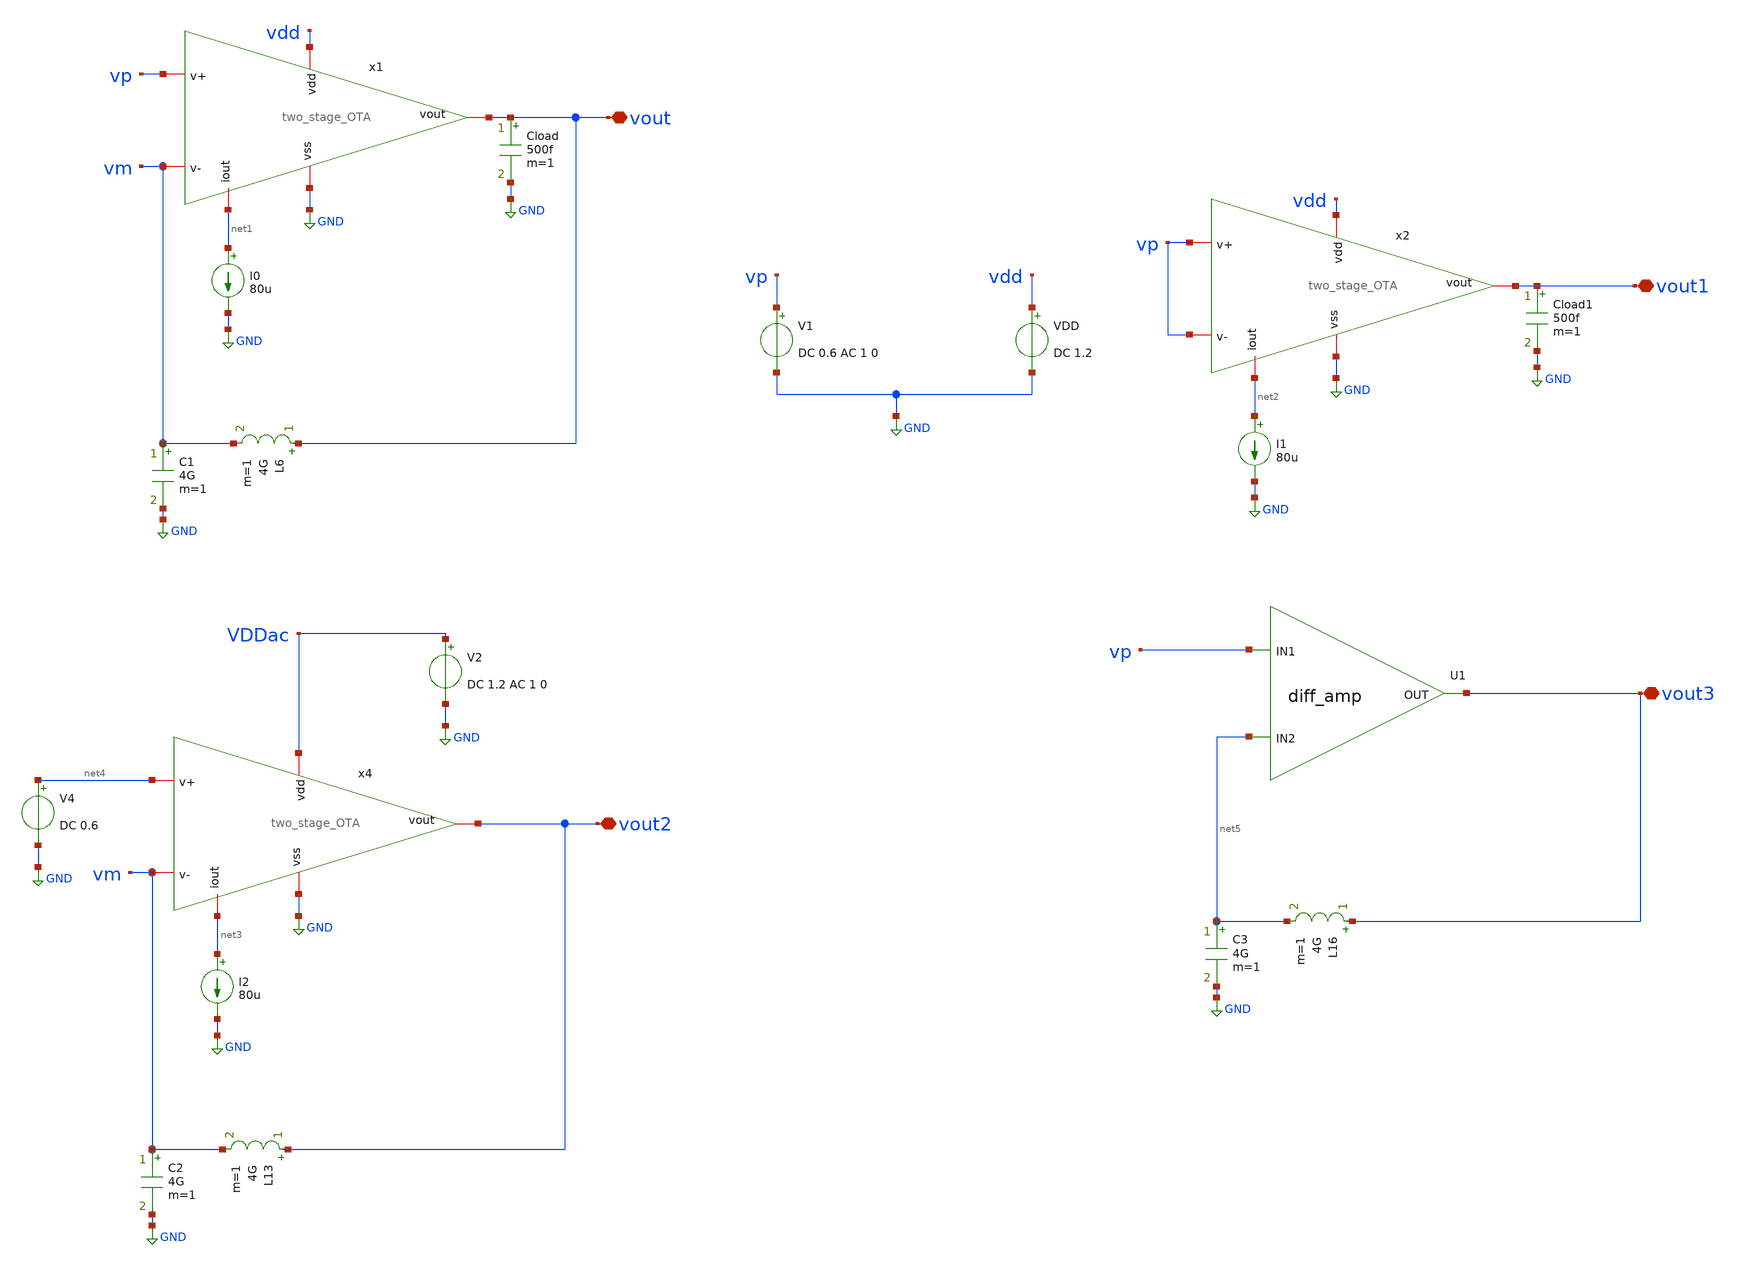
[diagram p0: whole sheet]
** sch_path: modules/module_1_bandgap_reference/part_1_OTA/testbenches/ota_testbench.sch
**.subckt ota_testbench vout vout1 vout2 vout3
*.iopin vout
*.iopin vout1
*.iopin vout2
*.iopin vout3
V1 vp GND DC 0.6 AC 1 0
VDD vdd GND DC 1.2
I0 net1 GND 80u
Cload vout GND 500f m=1
L6 vout vm 4G m=1
C1 vm GND 4G m=1
I1 net2 GND 80u
Cload1 vout1 GND 500f m=1
I2 net3 GND 80u
L13 vout2 vm 4G m=1
C2 vm GND 4G m=1
V2 VDDac GND DC 1.2 AC 1 0
V4 net4 GND DC 0.6
XU1 vout3 vp net5 diff_amp_cell
L16 vout3 net5 4G m=1
C3 net5 GND 4G m=1
x4 VDDac net3 net4 vm vout2 GND two_stage_OTA
x1 vdd net1 vp vm vout GND two_stage_OTA
x2 vdd net2 vp vp vout1 GND two_stage_OTA
**** begin user architecture code

.lib $::SG13G2_MODELS/cornerCAP.lib cap_typ
.lib cornerMOSlv.lib mos_tt



.control
op
save all
write tb_OTA_op.raw
.endc

.control
op
ac dec 100 1 10e6
save all
let Av = db(v(vout))
let PSRR = db(v(vout2)/v(VDDac))
let CMRR = db((v(vout)/v(vp))/(v(vout1)/v(vp)))
let phase = 180*cph(vout)/pi
write output_file.raw
.endc


**** end user architecture code
**.ends

* expanding   symbol:
*+  /home/pedersen/projects/IHP-AnalogAcademy/modules/module_1_bandgap_reference/part_1_OTA/schematic/two_stage_OTA.sym # of pins=6
** sym_path: /home/pedersen/projects/IHP-AnalogAcademy/modules/module_1_bandgap_reference/part_1_OTA/schematic/two_stage_OTA.sym
** sch_path: /home/pedersen/projects/IHP-AnalogAcademy/modules/module_1_bandgap_reference/part_1_OTA/schematic/two_stage_OTA.sch
.subckt two_stage_OTA vdd iout v+ v- vout vss
*.iopin v-
*.iopin v+
*.iopin vss
*.iopin vdd
*.iopin iout
*.iopin vout
XM4 vss net1 net3 vss sg13_lv_nmos w=720n l=9.75u ng=1 m=1 mm_ok=1
XM3 vss net1 net1 vss sg13_lv_nmos w=720n l=9.75u ng=1 m=1 mm_ok=1
XM1 net1 v- net2 vdd sg13_lv_pmos w=7.41u l=3.64u ng=1 m=1 mm_ok=1
XM2 net3 v+ net2 vdd sg13_lv_pmos w=7.41u l=3.64u ng=1 m=1 mm_ok=1
XM5 net2 iout vdd vdd sg13_lv_pmos w=5.3u l=1.95u ng=1 m=1 mm_ok=1
XM7 vout iout vdd vdd sg13_lv_pmos w=75u l=2.08u ng=8 m=1 mm_ok=1
XM6 vss net3 vout vss sg13_lv_nmos w=28.8u l=9.75u ng=4 m=1 mm_ok=1
XM9 iout iout vdd vdd sg13_lv_pmos w=75u l=2.08u ng=8 m=1 mm_ok=1
XC2 net3 vout cap_cmim w=22.295e-6 l=22.295e-6 m=1 mm_ok=1
.ends

.GLOBAL GND
**** begin user architecture code


.subckt diff_amp_cell OUT IN1 IN2

N1 out in1 in2 diff_amp_model

.ends diff_amp_cell



.model diff_amp_model diff_amp



.control

* following line specifies the location for the .osdi file so ngspice can use it.

pre_osdi
+ /home/pedersen/chipdesign/cmos_analog/opensource_analog_course/bgr_bjt/verilog/diff_amp.osdi

.endc


**** end user architecture code
.end
